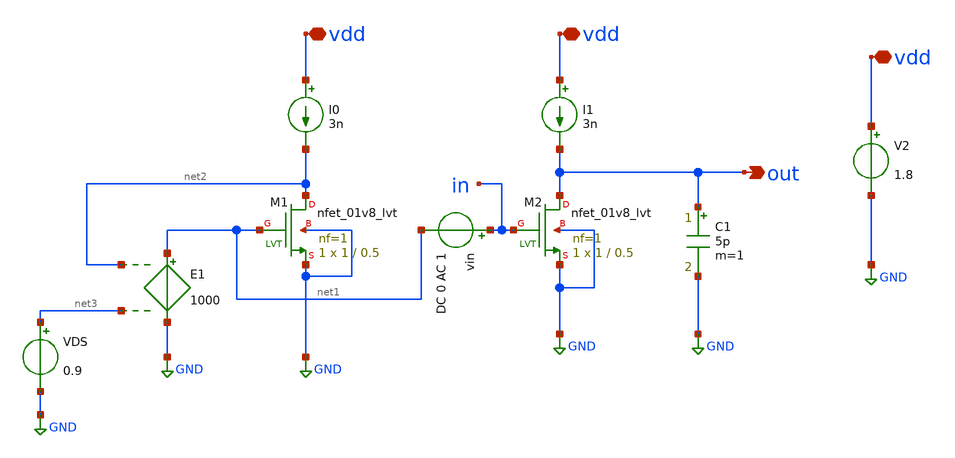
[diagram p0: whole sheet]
** sch_path: Simple-CS-Amplifier/csamp3.sch
**.subckt csamp3 vdd vdd vdd out
*.iopin vdd
*.iopin vdd
*.iopin vdd
*.opin out
XM1 net2 net1 GND GND sky130_fd_pr__nfet_01v8_lvt L=0.5 W=1 nf=1 ad='int((nf+1)/2) * W/nf * 0.29' as='int((nf+2)/2) * W/nf * 0.29'
+ pd='2*int((nf+1)/2) * (W/nf + 0.29)' ps='2*int((nf+2)/2) * (W/nf + 0.29)' nrd='0.29 / W' nrs='0.29 / W'
+ sa=0 sb=0 sd=0 mult=1 m=1
E1 net1 GND net2 net3 1000
I0 vdd net2 3n
VDS net3 GND 0.9
V2 vdd GND 1.8
XM2 out in GND GND sky130_fd_pr__nfet_01v8_lvt L=0.5 W=1 nf=1 ad='int((nf+1)/2) * W/nf * 0.29' as='int((nf+2)/2) * W/nf * 0.29'
+ pd='2*int((nf+1)/2) * (W/nf + 0.29)' ps='2*int((nf+2)/2) * (W/nf + 0.29)' nrd='0.29 / W' nrs='0.29 / W'
+ sa=0 sb=0 sd=0 mult=1 m=1
I1 vdd out 3n
vin in net1 DC 0 AC 1
C1 out GND 5p m=1
**** begin user architecture code



.lib /usr/local/share/pdk/sky130A/libs.tech/ngspice/sky130.lib.spice tt
.option wnflag=1 scale=1e-6

.control
save all

*save @m.xm2.msky130_fd_pr__nfet_01v8_lvt[vgs]
*save @m.xm2.msky130_fd_pr__nfet_01v8_lvt[vds]
*save @m.xm2.msky130_fd_pr__nfet_01v8_lvt[gm]
*save @m.xm2.msky130_fd_pr__nfet_01v8_lvt[id]
*save @m.xm2.msky130_fd_pr__nfet_01v8_lvt[gds]
*save @m.xm2.msky130_fd_pr__nfet_01v8_lvt[cgg]

AC dec 10 1 100Meg

*let vgs = @m.xm2.msky130_fd_pr__nfet_01v8_lvt[vgs]
*let vds = @m.xm2.msky130_fd_pr__nfet_01v8_lvt[vds]
*let gm = @m.xm2.msky130_fd_pr__nfet_01v8_lvt[gm]
*let id = @m.xm2.msky130_fd_pr__nfet_01v8_lvt[id]
*let ro = 1/@m.xm2.msky130_fd_pr__nfet_01v8_lvt[gds]
*let cgg = @m.xm2.msky130_fd_pr__nfet_01v8_lvt[cgg]

*let ao = gm*ro
*let ft = gm/(2*pi*cgg)
*plot v(out)

*tran 10u 10m

*plot ao



*wrdata ao-L=0.40.txt ao
.endc


**** end user architecture code
**.ends
.GLOBAL GND
.end
